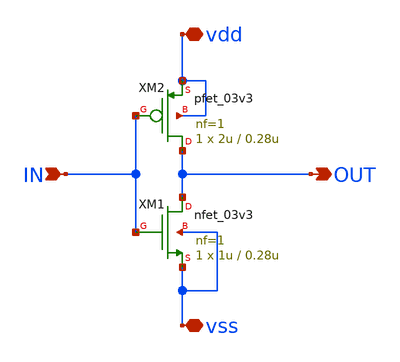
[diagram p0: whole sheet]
** sch_path: CAD6/DFF_Ray/INV.sch
**.subckt INV IN OUT vss vdd
*.ipin IN
*.opin OUT
*.iopin vss
*.iopin vdd
XM1 OUT IN vss vss nfet_03v3 L=0.28u W=1u nf=1 ad='int((nf+1)/2) * W/nf * 0.18u' as='int((nf+2)/2) * W/nf * 0.18u'
+ pd='2*int((nf+1)/2) * (W/nf + 0.18u)' ps='2*int((nf+2)/2) * (W/nf + 0.18u)' nrd='0.18u / W' nrs='0.18u / W'
+ sa=0 sb=0 sd=0 m=1
XM2 OUT IN vdd vdd pfet_03v3 L=0.28u W=2u nf=1 ad='int((nf+1)/2) * W/nf * 0.18u' as='int((nf+2)/2) * W/nf * 0.18u'
+ pd='2*int((nf+1)/2) * (W/nf + 0.18u)' ps='2*int((nf+2)/2) * (W/nf + 0.18u)' nrd='0.18u / W' nrs='0.18u / W'
+ sa=0 sb=0 sd=0 m=1
**.ends
.end
